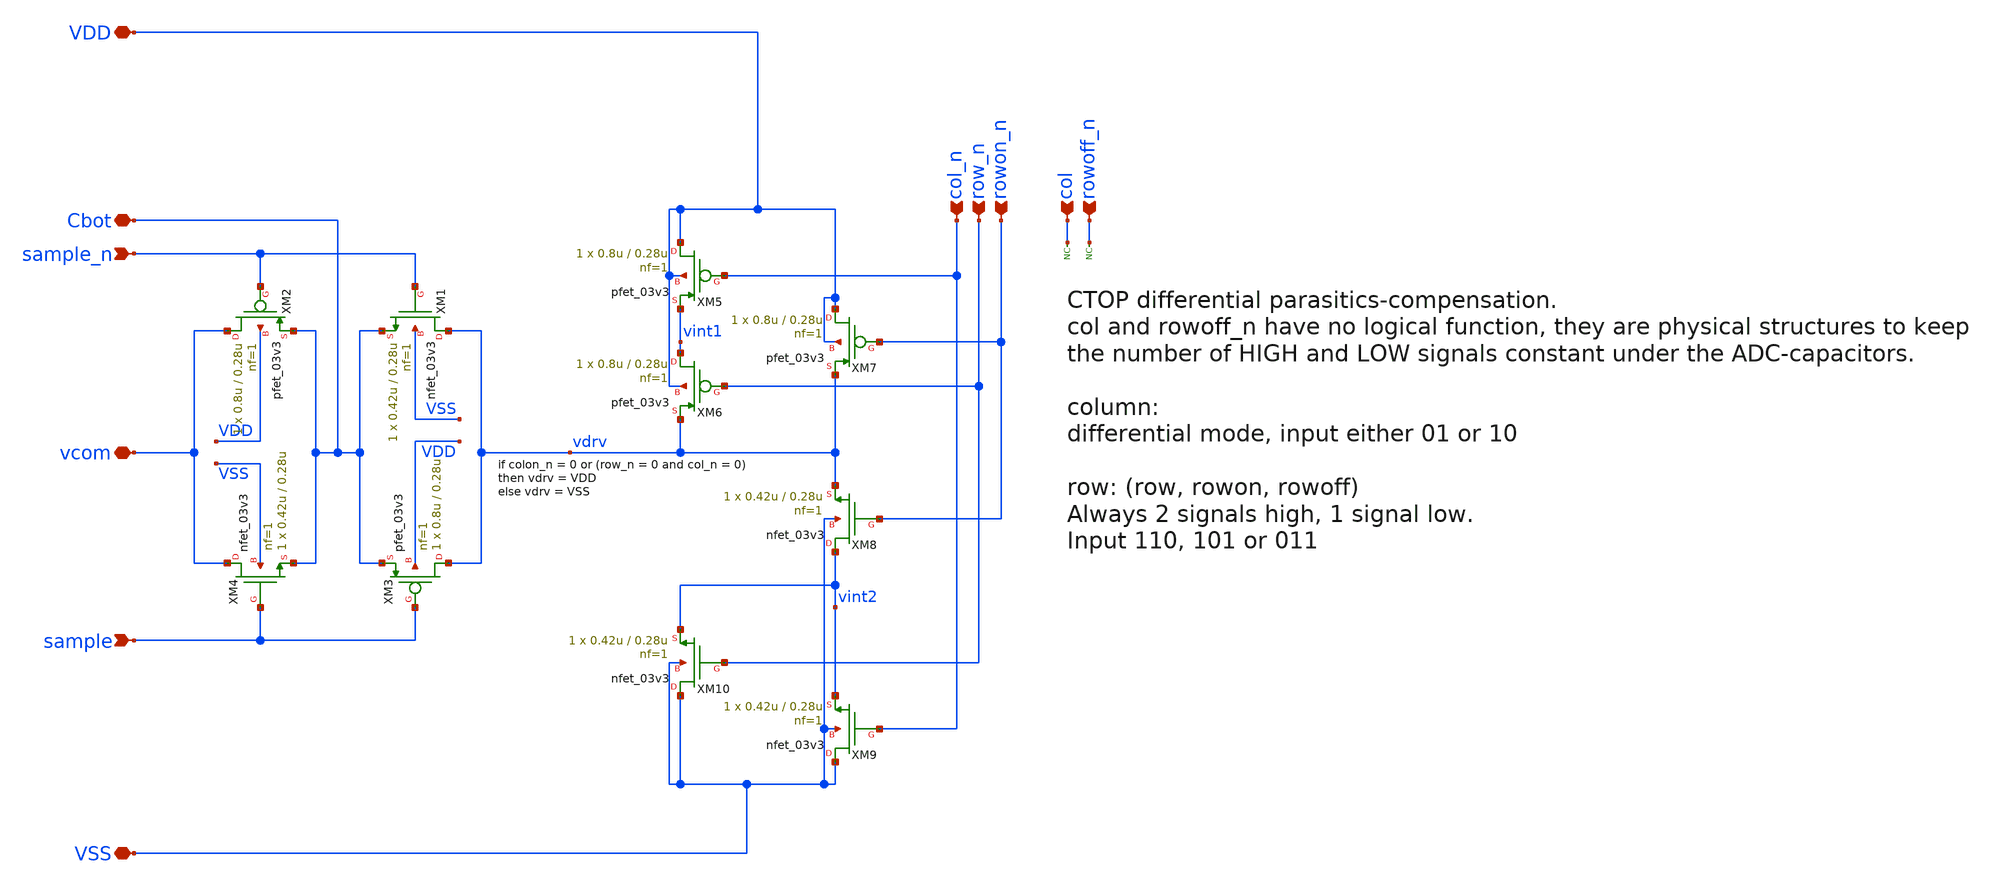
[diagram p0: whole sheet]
** sch_path: adc_sar_array_circuit_8.sch
**.subckt adc_sar_array_circuit_8 sample_n sample vcom col_n row_n rowon_n VDD VSS Cbot col rowoff_n
*.ipin sample_n
*.ipin sample
*.iopin vcom
*.ipin col_n
*.ipin row_n
*.ipin rowon_n
*.iopin VDD
*.iopin VSS
*.iopin Cbot
*.ipin col
*.ipin rowoff_n
* noconn col
* noconn rowoff_n
XM1 vdrv sample_n Cbot VSS nfet_03v3 L=0.28u W=0.42u nf=1 ad='int((nf+1)/2) * W/nf * 0.18u' as='int((nf+2)/2) * W/nf * 0.18u'
+ pd='2*int((nf+1)/2) * (W/nf + 0.18u)' ps='2*int((nf+2)/2) * (W/nf + 0.18u)' nrd='0.18u / W' nrs='0.18u / W'
+ sa=0 sb=0 sd=0 m=1
XM2 vcom sample_n Cbot VDD pfet_03v3 L=0.28u W=0.8u nf=1 ad='int((nf+1)/2) * W/nf * 0.18u' as='int((nf+2)/2) * W/nf * 0.18u'
+ pd='2*int((nf+1)/2) * (W/nf + 0.18u)' ps='2*int((nf+2)/2) * (W/nf + 0.18u)' nrd='0.18u / W' nrs='0.18u / W'
+ sa=0 sb=0 sd=0 m=1
XM3 vdrv sample Cbot VDD pfet_03v3 L=0.28u W=0.8u nf=1 ad='int((nf+1)/2) * W/nf * 0.18u' as='int((nf+2)/2) * W/nf * 0.18u'
+ pd='2*int((nf+1)/2) * (W/nf + 0.18u)' ps='2*int((nf+2)/2) * (W/nf + 0.18u)' nrd='0.18u / W' nrs='0.18u / W'
+ sa=0 sb=0 sd=0 m=1
XM4 vcom sample Cbot VSS nfet_03v3 L=0.28u W=0.42u nf=1 ad='int((nf+1)/2) * W/nf * 0.18u' as='int((nf+2)/2) * W/nf * 0.18u'
+ pd='2*int((nf+1)/2) * (W/nf + 0.18u)' ps='2*int((nf+2)/2) * (W/nf + 0.18u)' nrd='0.18u / W' nrs='0.18u / W'
+ sa=0 sb=0 sd=0 m=1
XM5 VDD col_n vint1 VDD pfet_03v3 L=0.28u W=0.8u nf=1 ad='int((nf+1)/2) * W/nf * 0.18u' as='int((nf+2)/2) * W/nf * 0.18u'
+ pd='2*int((nf+1)/2) * (W/nf + 0.18u)' ps='2*int((nf+2)/2) * (W/nf + 0.18u)' nrd='0.18u / W' nrs='0.18u / W'
+ sa=0 sb=0 sd=0 m=1
XM6 vint1 row_n vdrv VDD pfet_03v3 L=0.28u W=0.8u nf=1 ad='int((nf+1)/2) * W/nf * 0.18u' as='int((nf+2)/2) * W/nf * 0.18u'
+ pd='2*int((nf+1)/2) * (W/nf + 0.18u)' ps='2*int((nf+2)/2) * (W/nf + 0.18u)' nrd='0.18u / W' nrs='0.18u / W'
+ sa=0 sb=0 sd=0 m=1
XM7 VDD rowon_n vdrv VDD pfet_03v3 L=0.28u W=0.8u nf=1 ad='int((nf+1)/2) * W/nf * 0.18u' as='int((nf+2)/2) * W/nf * 0.18u'
+ pd='2*int((nf+1)/2) * (W/nf + 0.18u)' ps='2*int((nf+2)/2) * (W/nf + 0.18u)' nrd='0.18u / W' nrs='0.18u / W'
+ sa=0 sb=0 sd=0 m=1
XM8 vint2 rowon_n vdrv VSS nfet_03v3 L=0.28u W=0.42u nf=1 ad='int((nf+1)/2) * W/nf * 0.18u' as='int((nf+2)/2) * W/nf * 0.18u'
+ pd='2*int((nf+1)/2) * (W/nf + 0.18u)' ps='2*int((nf+2)/2) * (W/nf + 0.18u)' nrd='0.18u / W' nrs='0.18u / W'
+ sa=0 sb=0 sd=0 m=1
XM9 VSS col_n vint2 VSS nfet_03v3 L=0.28u W=0.42u nf=1 ad='int((nf+1)/2) * W/nf * 0.18u' as='int((nf+2)/2) * W/nf * 0.18u'
+ pd='2*int((nf+1)/2) * (W/nf + 0.18u)' ps='2*int((nf+2)/2) * (W/nf + 0.18u)' nrd='0.18u / W' nrs='0.18u / W'
+ sa=0 sb=0 sd=0 m=1
XM10 VSS row_n vint2 VSS nfet_03v3 L=0.28u W=0.42u nf=1 ad='int((nf+1)/2) * W/nf * 0.18u' as='int((nf+2)/2) * W/nf * 0.18u'
+ pd='2*int((nf+1)/2) * (W/nf + 0.18u)' ps='2*int((nf+2)/2) * (W/nf + 0.18u)' nrd='0.18u / W' nrs='0.18u / W'
+ sa=0 sb=0 sd=0 m=1
**.ends
.end
